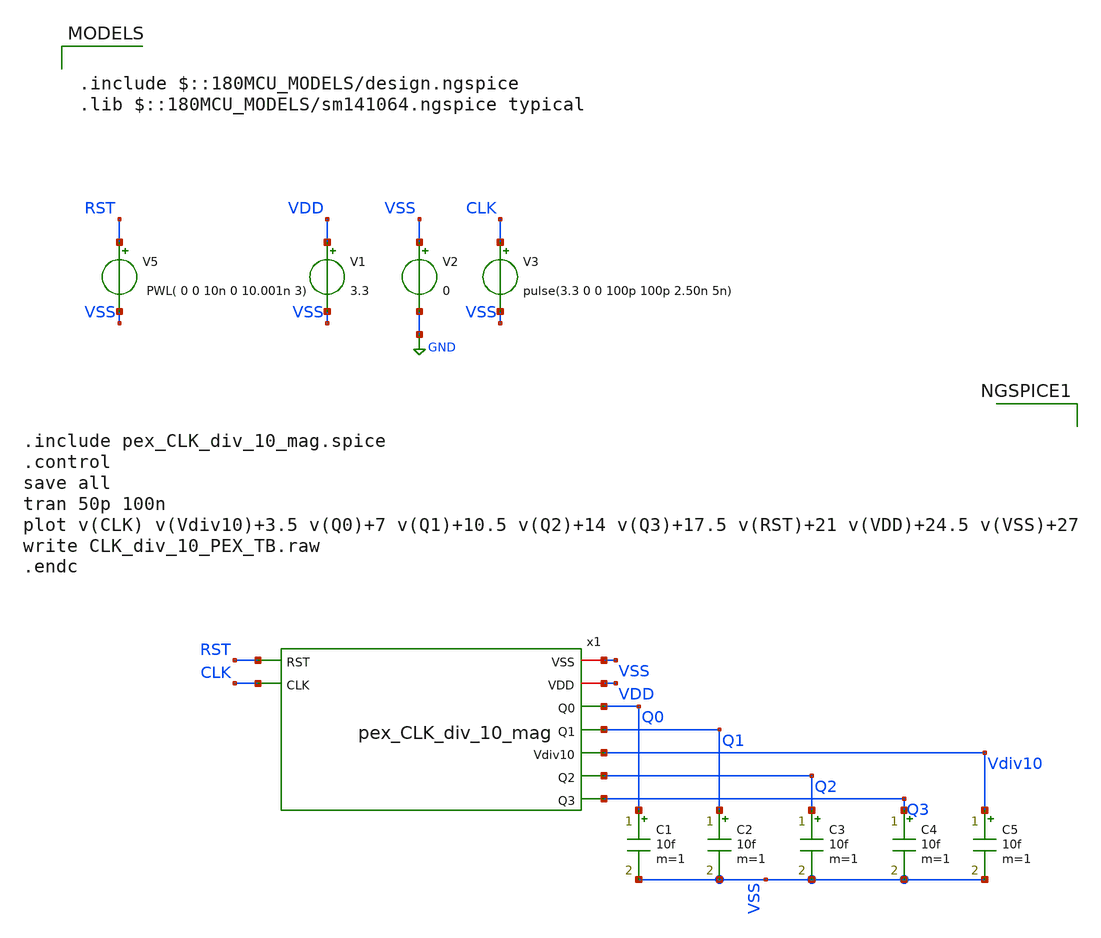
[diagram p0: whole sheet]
** sch_path: Clock_Generator_PAKISTAN_02/Schematics/CLK_div_10_PEX_TB.sch
**.subckt CLK_div_10_PEX_TB
V1 VDD VSS 3.3
V2 VSS GND 0
V3 CLK VSS pulse(3.3 0 0 100p 100p 2.50n 5n)
C1 Q0 VSS 10f m=1
C2 Q1 VSS 10f m=1
C3 Q2 VSS 10f m=1
C4 Q3 VSS 10f m=1
C5 Vdiv10 VSS 10f m=1
V5 RST VSS PWL( 0 0 10n 0 10.001n 3)
x1 VSS VDD Q0 Q1 RST Vdiv10 Q2 Q3 CLK pex_CLK_div_10_mag
**** begin user architecture code

.include $::180MCU_MODELS/design.ngspice
.lib $::180MCU_MODELS/sm141064.ngspice typical



.include pex_CLK_div_10_mag.spice
.control
save all
tran 50p 100n
plot v(CLK) v(Vdiv10)+3.5 v(Q0)+7 v(Q1)+10.5 v(Q2)+14 v(Q3)+17.5 v(RST)+21 v(VDD)+24.5 v(VSS)+27
write CLK_div_10_PEX_TB.raw
.endc


**** end user architecture code
**.ends
.GLOBAL GND
.end
